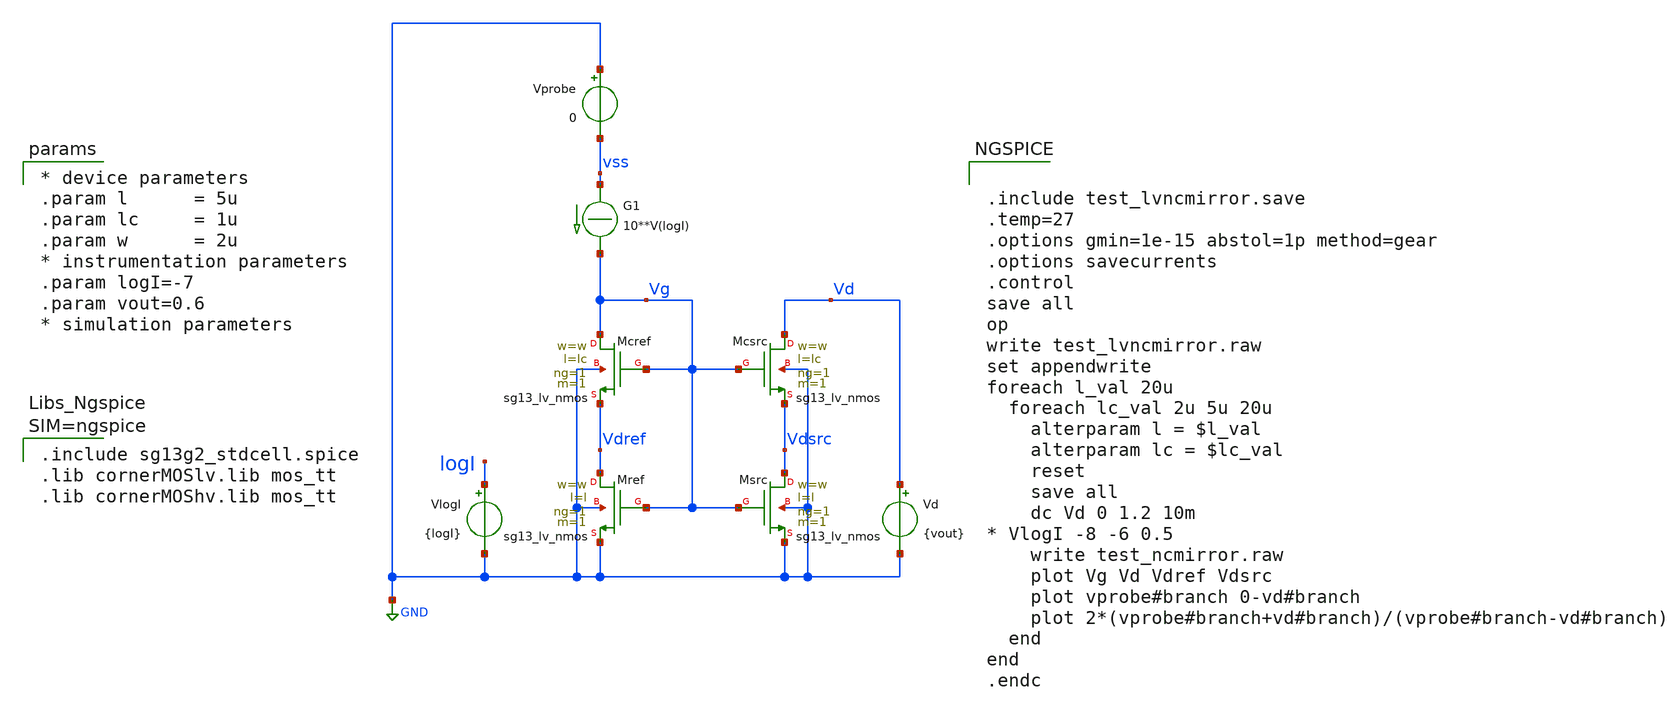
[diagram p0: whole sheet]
** sch_path: xschem/test_lvncmirror.sch
**.subckt test_lvncmirror
XMsrc Vdsrc Vg GND GND sg13_lv_nmos w=w l=l ng=1 m=1 mm_ok=1
XMref Vdref Vg GND GND sg13_lv_nmos w=w l=l ng=1 m=1 mm_ok=1
Vprobe GND vss 0
.save i(vprobe)
G1 vss Vg CUR=' 10**V(logI) '
VlogI logI GND {logI}
.save i(vlogi)
Vd Vd GND {vout}
.save i(vd)
XMcsrc Vd Vg Vdsrc GND sg13_lv_nmos w=w l=lc ng=1 m=1 mm_ok=1
XMcref Vg Vg Vdref GND sg13_lv_nmos w=w l=lc ng=1 m=1 mm_ok=1
**** begin user architecture code


.include sg13g2_stdcell.spice
.lib cornerMOSlv.lib mos_tt
.lib cornerMOShv.lib mos_tt



* device parameters
.param l      = 5u
.param lc     = 1u
.param w      = 2u
* instrumentation parameters
.param logI=-7
.param vout=0.6
* simulation parameters




.include test_lvncmirror.save
.temp=27
.options gmin=1e-15 abstol=1p method=gear
.options savecurrents
.control
save all
op
write test_lvncmirror.raw
set appendwrite
foreach l_val 20u
  foreach lc_val 2u 5u 20u
    alterparam l = $l_val
    alterparam lc = $lc_val
    reset
    save all
    dc Vd 0 1.2 10m
* VlogI -8 -6 0.5
    write test_ncmirror.raw
    plot Vg Vd Vdref Vdsrc
    plot vprobe#branch 0-vd#branch
    plot 2*(vprobe#branch+vd#branch)/(vprobe#branch-vd#branch)
  end
end
.endc


**** end user architecture code
**.ends
.GLOBAL GND
.end
